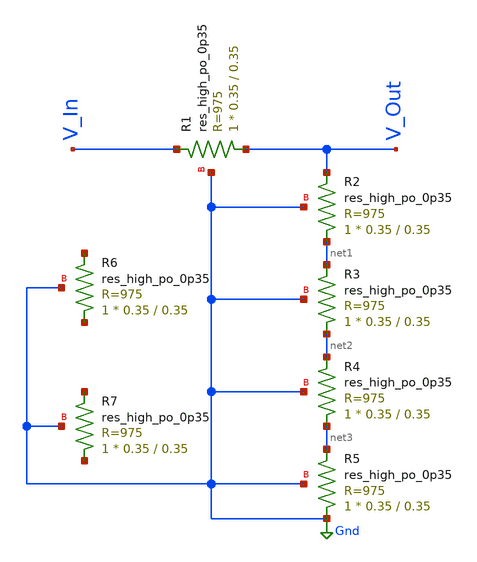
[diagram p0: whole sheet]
** sch_path: Schematic/VoltageDivider.sch
**.subckt VoltageDivider
XR1 V_Out V_In Gnd sky130_fd_pr__res_high_po_0p35 L=0.35 mult=1 m=1
XR2 net1 V_Out Gnd sky130_fd_pr__res_high_po_0p35 L=0.35 mult=1 m=1
XR3 net2 net1 Gnd sky130_fd_pr__res_high_po_0p35 L=0.35 mult=1 m=1
XR4 net3 net2 Gnd sky130_fd_pr__res_high_po_0p35 L=0.35 mult=1 m=1
XR5 Gnd net3 Gnd sky130_fd_pr__res_high_po_0p35 L=0.35 mult=1 m=1
XR6 net4 net5 Gnd sky130_fd_pr__res_high_po_0p35 L=0.35 mult=1 m=1
XR7 net6 net7 Gnd sky130_fd_pr__res_high_po_0p35 L=0.35 mult=1 m=1
**.ends
.GLOBAL Gnd
.end
